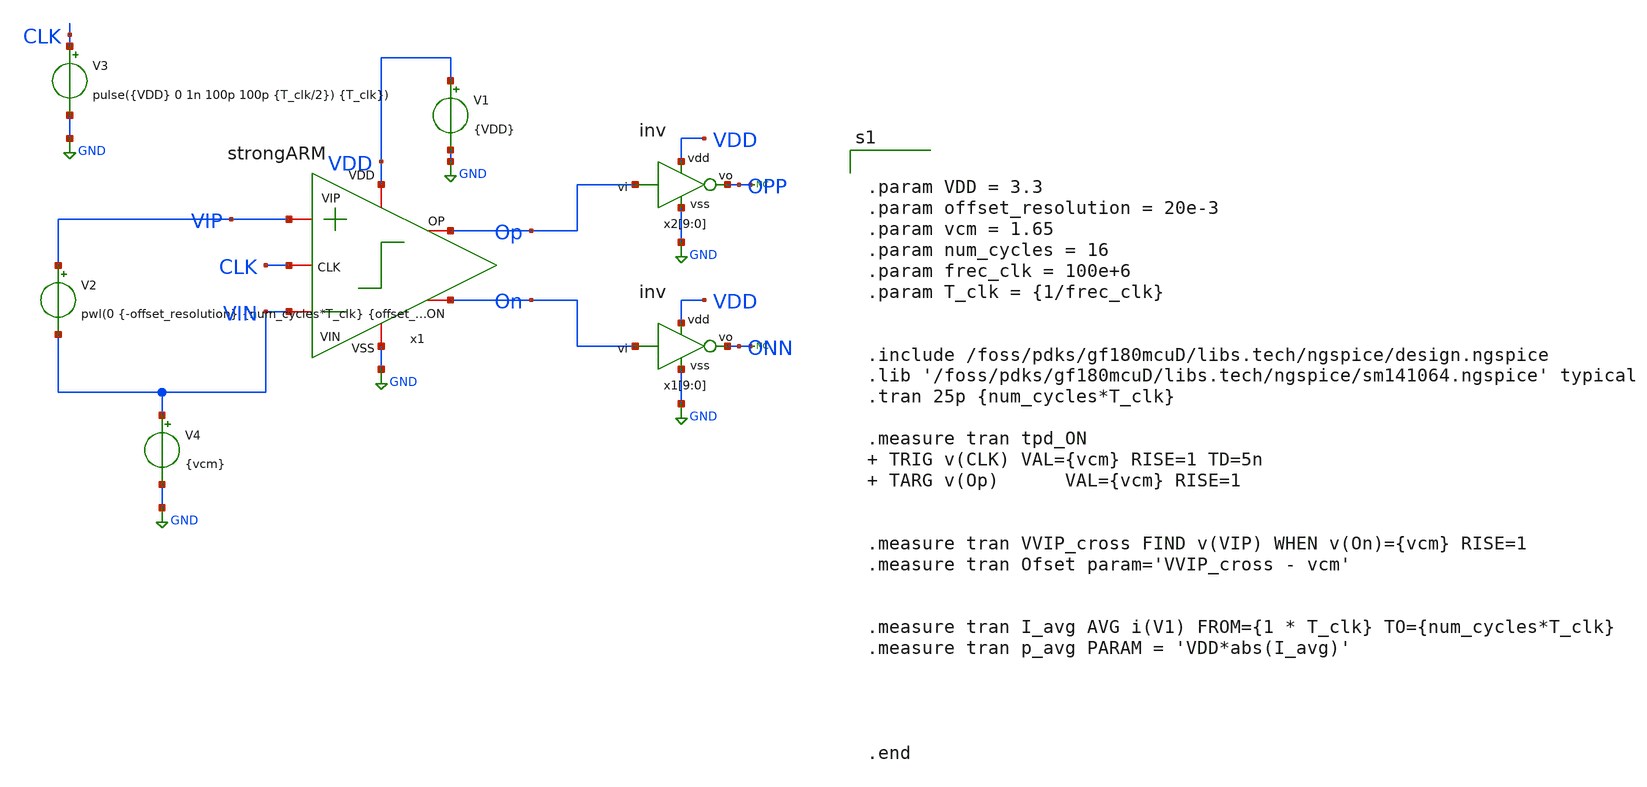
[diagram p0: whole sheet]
** sch_path: designs/sar_adc/comparator/Testbench/tb_strongARM_offset.sch
**.subckt tb_strongARM_offset
V1 VDD GND {VDD}
V2 VIP VIN pwl(0 {-offset_resolution} {num_cycles*T_clk} {offset_resolution})
V3 CLK GND pulse({VDD} 0 1n 100p 100p {T_clk/2}) {T_clk})
V4 VIN GND {vcm}
x1 VDD CLK On Op VIN VIP GND strongARM
x2[9] VDD Op OPP GND inv
x2[8] VDD Op OPP GND inv
x2[7] VDD Op OPP GND inv
x2[6] VDD Op OPP GND inv
x2[5] VDD Op OPP GND inv
x2[4] VDD Op OPP GND inv
x2[3] VDD Op OPP GND inv
x2[2] VDD Op OPP GND inv
x2[1] VDD Op OPP GND inv
x2[0] VDD Op OPP GND inv
x1[9] VDD On ONN GND inv
x1[8] VDD On ONN GND inv
x1[7] VDD On ONN GND inv
x1[6] VDD On ONN GND inv
x1[5] VDD On ONN GND inv
x1[4] VDD On ONN GND inv
x1[3] VDD On ONN GND inv
x1[2] VDD On ONN GND inv
x1[1] VDD On ONN GND inv
x1[0] VDD On ONN GND inv
* noconn ONN
* noconn OPP
**** begin user architecture code


.param VDD = 3.3
.param offset_resolution = 20e-3
.param vcm = 1.65
.param num_cycles = 16
.param frec_clk = 100e+6
.param T_clk = {1/frec_clk}


.include /foss/pdks/gf180mcuD/libs.tech/ngspice/design.ngspice
.lib '/foss/pdks/gf180mcuD/libs.tech/ngspice/sm141064.ngspice' typical
.tran 25p {num_cycles*T_clk}

.measure tran tpd_ON  TRIG v(CLK) VAL={vcm} RISE=1 TD=5n  TARG v(Op)      VAL={vcm} RISE=1


.measure tran VVIP_cross FIND v(VIP) WHEN v(On)={vcm} RISE=1
.measure tran Ofset param='VVIP_cross - vcm'


.measure tran I_avg AVG i(V1) FROM={1 * T_clk} TO={num_cycles*T_clk}
.measure tran p_avg PARAM = 'VDD*abs(I_avg)'




.end


**** end user architecture code
**.ends
.GLOBAL GND
.end
